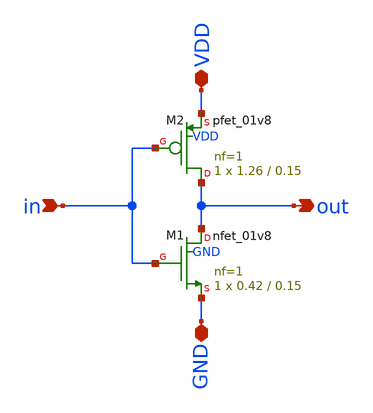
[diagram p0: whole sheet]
** sch_path: xschem/charge_pumps2/inverter.sch
**.subckt inverter in out GND VDD
*.ipin in
*.opin out
*.iopin GND
*.iopin VDD
XM1 out in GND GND sky130_fd_pr__nfet_01v8 L=0.15 W=0.42 nf=1 ad='int((nf+1)/2) * W/nf * 0.29' as='int((nf+2)/2) * W/nf * 0.29'
+ pd='2*int((nf+1)/2) * (W/nf + 0.29)' ps='2*int((nf+2)/2) * (W/nf + 0.29)' nrd='0.29 / W' nrs='0.29 / W'
+ sa=0 sb=0 sd=0 mult=1 m=1
XM2 out in VDD VDD sky130_fd_pr__pfet_01v8 L=0.15 W=1.26 nf=1 ad='int((nf+1)/2) * W/nf * 0.29' as='int((nf+2)/2) * W/nf * 0.29'
+ pd='2*int((nf+1)/2) * (W/nf + 0.29)' ps='2*int((nf+2)/2) * (W/nf + 0.29)' nrd='0.29 / W' nrs='0.29 / W'
+ sa=0 sb=0 sd=0 mult=1 m=1
**.ends
.end
